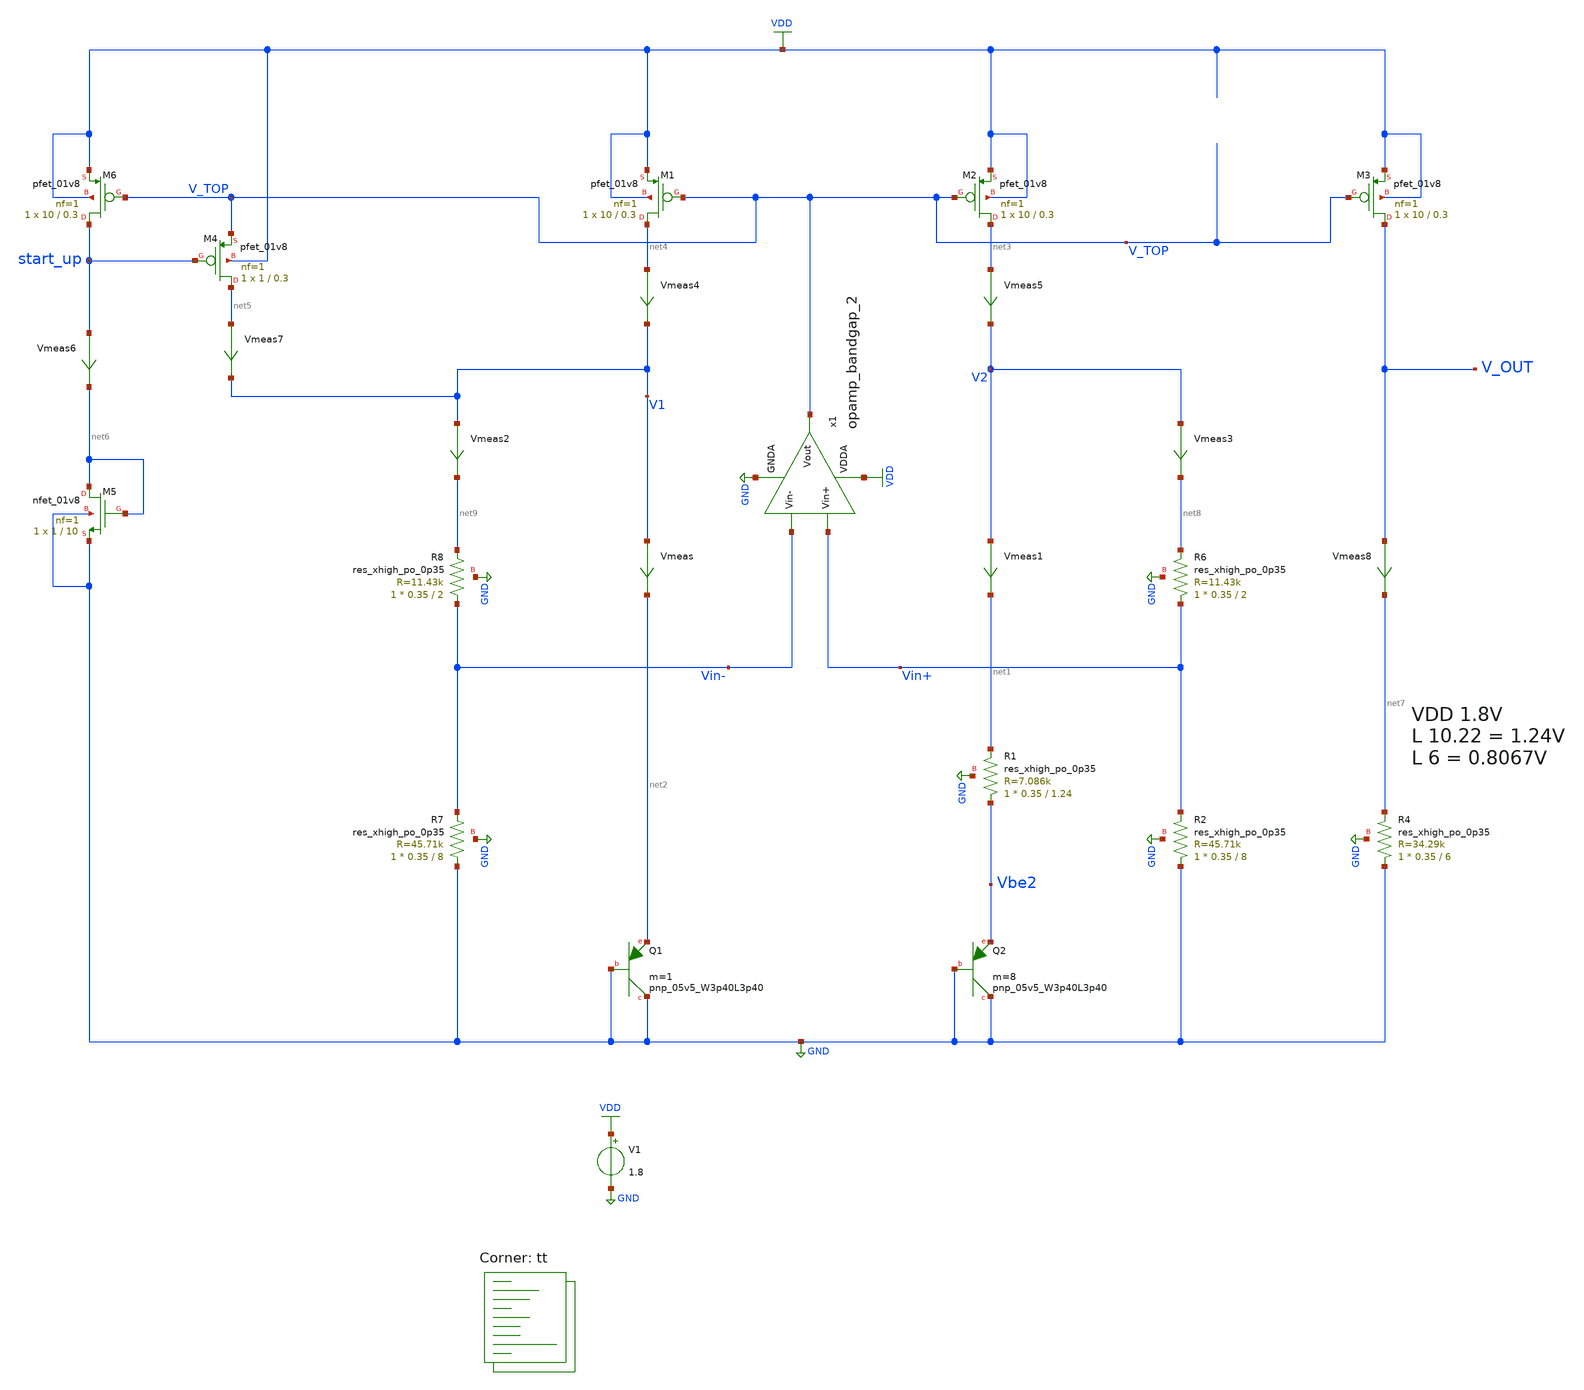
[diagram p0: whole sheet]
** sch_path: projects/bandgapref/xschem_ngspice/new_files/tb_low_voltage_BGR_9.sch
**.subckt tb_low_voltage_BGR_9
V1 VDD GND 1.8
XQ1 GND GND net2 sky130_fd_pr__pnp_05v5_W3p40L3p40 m=1
XQ2 GND GND Vbe2 sky130_fd_pr__pnp_05v5_W3p40L3p40 m=8
XM1 net4 V_TOP VDD VDD sky130_fd_pr__pfet_01v8 L=0.3 W=10 nf=1 ad='int((nf+1)/2) * W/nf * 0.29' as='int((nf+2)/2) * W/nf * 0.29'
+ pd='2*int((nf+1)/2) * (W/nf + 0.29)' ps='2*int((nf+2)/2) * (W/nf + 0.29)' nrd='0.29 / W' nrs='0.29 / W'
+ sa=0 sb=0 sd=0 mult=1 m=1
XM2 net3 V_TOP VDD VDD sky130_fd_pr__pfet_01v8 L=0.3 W=10 nf=1 ad='int((nf+1)/2) * W/nf * 0.29' as='int((nf+2)/2) * W/nf * 0.29'
+ pd='2*int((nf+1)/2) * (W/nf + 0.29)' ps='2*int((nf+2)/2) * (W/nf + 0.29)' nrd='0.29 / W' nrs='0.29 / W'
+ sa=0 sb=0 sd=0 mult=1 m=1
XM3 V_OUT V_TOP VDD VDD sky130_fd_pr__pfet_01v8 L=0.3 W=10 nf=1 ad='int((nf+1)/2) * W/nf * 0.29' as='int((nf+2)/2) * W/nf * 0.29'
+ pd='2*int((nf+1)/2) * (W/nf + 0.29)' ps='2*int((nf+2)/2) * (W/nf + 0.29)' nrd='0.29 / W' nrs='0.29 / W'
+ sa=0 sb=0 sd=0 mult=1 m=1
Vmeas V1 net2 0
.save i(vmeas)
Vmeas1 V2 net1 0
.save i(vmeas1)
Vmeas2 V1 net9 0
.save i(vmeas2)
XR1 Vbe2 net1 GND sky130_fd_pr__res_xhigh_po_0p35 L=1.24 mult=1 m=1
XR2 GND Vin+ GND sky130_fd_pr__res_xhigh_po_0p35 L=8 mult=1 m=1
XR4 GND net7 GND sky130_fd_pr__res_xhigh_po_0p35 L=6 mult=1 m=1
Vmeas3 V2 net8 0
.save i(vmeas3)
Vmeas4 net4 V1 0
.save i(vmeas4)
XM5 net6 net6 GND GND sky130_fd_pr__nfet_01v8 L=10 W=1 nf=1 ad='int((nf+1)/2) * W/nf * 0.29' as='int((nf+2)/2) * W/nf * 0.29'
+ pd='2*int((nf+1)/2) * (W/nf + 0.29)' ps='2*int((nf+2)/2) * (W/nf + 0.29)' nrd='0.29 / W' nrs='0.29 / W'
+ sa=0 sb=0 sd=0 mult=1 m=1
XM6 start_up V_TOP VDD VDD sky130_fd_pr__pfet_01v8 L=0.3 W=10 nf=1 ad='int((nf+1)/2) * W/nf * 0.29' as='int((nf+2)/2) * W/nf * 0.29'
+ pd='2*int((nf+1)/2) * (W/nf + 0.29)' ps='2*int((nf+2)/2) * (W/nf + 0.29)' nrd='0.29 / W' nrs='0.29 / W'
+ sa=0 sb=0 sd=0 mult=1 m=1
Vmeas5 net3 V2 0
.save i(vmeas5)
XM4 net5 start_up V_TOP VDD sky130_fd_pr__pfet_01v8 L=0.3 W=1 nf=1 ad='int((nf+1)/2) * W/nf * 0.29' as='int((nf+2)/2) * W/nf * 0.29'
+ pd='2*int((nf+1)/2) * (W/nf + 0.29)' ps='2*int((nf+2)/2) * (W/nf + 0.29)' nrd='0.29 / W' nrs='0.29 / W'
+ sa=0 sb=0 sd=0 mult=1 m=1
Vmeas7 net5 V1 0
.save i(vmeas7)
x1 VDD V_TOP Vin- Vin+ GND opamp_bandgap_2
XR6 Vin+ net8 GND sky130_fd_pr__res_xhigh_po_0p35 L=2 mult=1 m=1
XR7 GND Vin- GND sky130_fd_pr__res_xhigh_po_0p35 L=8 mult=1 m=1
Vmeas8 V_OUT net7 0
.save i(vmeas8)
XR8 Vin- net9 GND sky130_fd_pr__res_xhigh_po_0p35 L=2 mult=1 m=1
Vmeas6 start_up net6 0
.save i(vmeas6)
**** begin user architecture code
.lib $::SKYWATER_MODELS/sky130.lib.spice tt



.option method=gear
.option wnflag=1
.option savecurrents
* .temp =140

.save @m.xm1.msky130_fd_pr__pfet_01v8[gm] @m.xm1.msky130_fd_pr__pfet_01v8[vth] @m.xm1.msky130_fd_pr__pfet_01v8[vgs] @m.xm1.msky130_fd_pr__pfet_01v8[vds] @m.xm2.msky130_fd_pr__pfet_01v8[gm] @m.xm2.msky130_fd_pr__pfet_01v8[vth] @m.xm2.msky130_fd_pr__pfet_01v8[vgs] @m.xm2.msky130_fd_pr__pfet_01v8[vds] @m.xm3.msky130_fd_pr__pfet_01v8[gm] @m.xm4.msky130_fd_pr__pfet_01v8[gm] @m.xm4.msky130_fd_pr__pfet_01v8[vth] @m.xm5.msky130_fd_pr__nfet_01v8[gm] @m.xm5.msky130_fd_pr__nfet_01v8[vth] @m.xm6.msky130_fd_pr__pfet_01v8[gm] @m.xm6.msky130_fd_pr__pfet_01v8[vth] @m.xm7.msky130_fd_pr__nfet_01v8[gm] @m.xm7.msky130_fd_pr__nfet_01v8[vth] @m.xm8.msky130_fd_pr__nfet_01v8[gm] @m.xm8.msky130_fd_pr__nfet_01v8[vth] @m.xm9.msky130_fd_pr__nfet_01v8[gm] @m.xm9.msky130_fd_pr__nfet_01v8[vth] @m.x1.xm1.msky130_fd_pr__nfet_01v8[gm] @m.x1.xm2.msky130_fd_pr__nfet_01v8[gm] @m.x1.xm3.msky130_fd_pr__nfet_01v8[gm] @m.x1.xm4.msky130_fd_pr__nfet_01v8[gm] @m.x1.xm5.msky130_fd_pr__pfet_01v8[gm] @m.x1.xm6.msky130_fd_pr__nfet_01v8[gm] @m.x1.xm7.msky130_fd_pr__pfet_01v8[gm] @m.x1.xm8.msky130_fd_pr__pfet_01v8[gm]

* .ic v(vin-) = 0.8
* .ic v(vin+) = 0.8
* .ic v(v_top) = 1.8

.control

    save all
    * dc temp -40 120 5 V1 1.6 2.0 0.05
    * dc V1 1.7 1.9 0.001 temp -40 120 40
    dc V1 0.0 2.0 0.2 temp -40 120 40
    * dc V1 0 2.0 0.02
    * tran 1ns 8us
    remzerovec
    write tb_low_voltage_BGR_9.raw
    * write tb_low_voltage_BGR_9_2.raw
    * write tb_low_voltage_BGR_9_3.raw
.endc



**** end user architecture code
**.ends

* expanding   symbol:  opamp_bandgap_2.sym # of pins=5
** sym_path: projects/bandgapref/xschem_ngspice/new_files/opamp_bandgap_2.sym
** sch_path: projects/bandgapref/xschem_ngspice/new_files/opamp_bandgap_2.sch
.subckt opamp_bandgap_2 VDDA Vout Vin- Vin+ GNDA
*.ipin Vin+
*.opin Vout
*.ipin Vin-
*.ipin GNDA
*.ipin VDDA
XM1 V_p VDDA GNDA GNDA sky130_fd_pr__nfet_01v8 L=5 W=5 nf=1 ad='int((nf+1)/2) * W/nf * 0.29' as='int((nf+2)/2) * W/nf * 0.29'
+ pd='2*int((nf+1)/2) * (W/nf + 0.29)' ps='2*int((nf+2)/2) * (W/nf + 0.29)' nrd='0.29 / W' nrs='0.29 / W'
+ sa=0 sb=0 sd=0 mult=1 m=1
XM2 V_mirror Vin- V_p GNDA sky130_fd_pr__nfet_01v8 L=0.3 W=5 nf=1 ad='int((nf+1)/2) * W/nf * 0.29' as='int((nf+2)/2) * W/nf * 0.29'
+ pd='2*int((nf+1)/2) * (W/nf + 0.29)' ps='2*int((nf+2)/2) * (W/nf + 0.29)' nrd='0.29 / W' nrs='0.29 / W'
+ sa=0 sb=0 sd=0 mult=1 m=1
XM3 1st_Vout Vin+ V_p GNDA sky130_fd_pr__nfet_01v8 L=0.3 W=5 nf=1 ad='int((nf+1)/2) * W/nf * 0.29' as='int((nf+2)/2) * W/nf * 0.29'
+ pd='2*int((nf+1)/2) * (W/nf + 0.29)' ps='2*int((nf+2)/2) * (W/nf + 0.29)' nrd='0.29 / W' nrs='0.29 / W'
+ sa=0 sb=0 sd=0 mult=1 m=1
XM5 V_mirror V_mirror VDDA VDDA sky130_fd_pr__pfet_01v8 L=0.3 W=10 nf=2 ad='int((nf+1)/2) * W/nf * 0.29'
+ as='int((nf+2)/2) * W/nf * 0.29' pd='2*int((nf+1)/2) * (W/nf + 0.29)' ps='2*int((nf+2)/2) * (W/nf + 0.29)'
+ nrd='0.29 / W' nrs='0.29 / W' sa=0 sb=0 sd=0 mult=1 m=1
XM6 1st_Vout V_mirror VDDA VDDA sky130_fd_pr__pfet_01v8 L=0.3 W=10 nf=2 ad='int((nf+1)/2) * W/nf * 0.29'
+ as='int((nf+2)/2) * W/nf * 0.29' pd='2*int((nf+1)/2) * (W/nf + 0.29)' ps='2*int((nf+2)/2) * (W/nf + 0.29)'
+ nrd='0.29 / W' nrs='0.29 / W' sa=0 sb=0 sd=0 mult=1 m=1
XM4 Vout VDDA GNDA GNDA sky130_fd_pr__nfet_01v8 L=5 W=5 nf=1 ad='int((nf+1)/2) * W/nf * 0.29' as='int((nf+2)/2) * W/nf * 0.29'
+ pd='2*int((nf+1)/2) * (W/nf + 0.29)' ps='2*int((nf+2)/2) * (W/nf + 0.29)' nrd='0.29 / W' nrs='0.29 / W'
+ sa=0 sb=0 sd=0 mult=1 m=1
XM7 Vout 1st_Vout VDDA VDDA sky130_fd_pr__pfet_01v8 L=0.3 W=10 nf=2 ad='int((nf+1)/2) * W/nf * 0.29'
+ as='int((nf+2)/2) * W/nf * 0.29' pd='2*int((nf+1)/2) * (W/nf + 0.29)' ps='2*int((nf+2)/2) * (W/nf + 0.29)'
+ nrd='0.29 / W' nrs='0.29 / W' sa=0 sb=0 sd=0 mult=1 m=1
.ends

.GLOBAL GND
.GLOBAL VDD
.end
